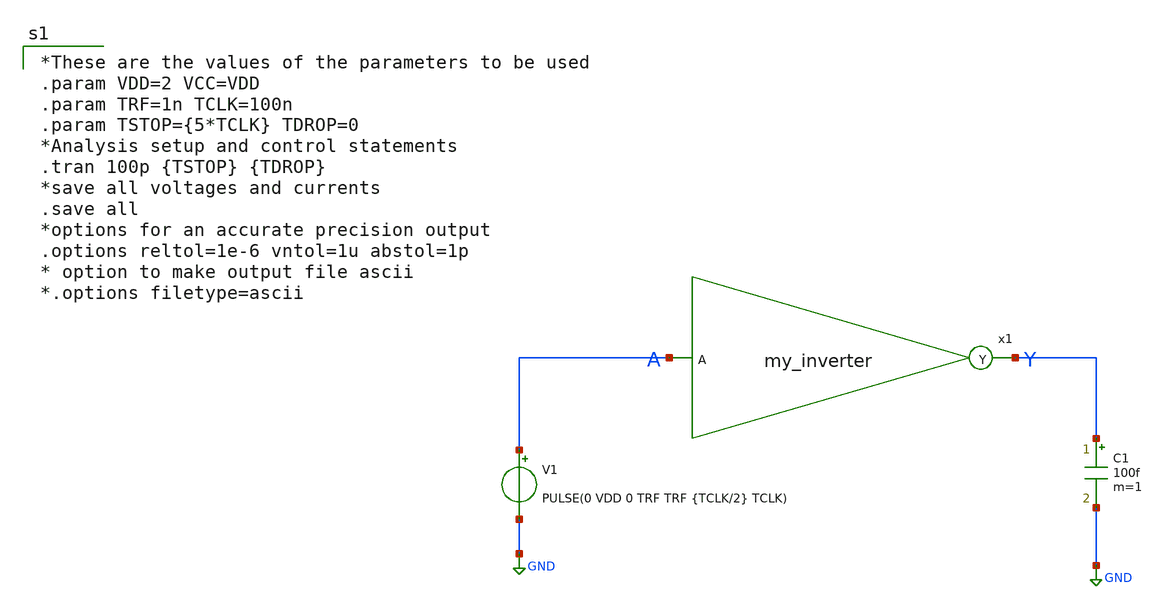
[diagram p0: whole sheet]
** sch_path: Lab4_test_bench.sch
**.subckt Lab4_test_bench
V1 A GND PULSE(0 VDD 0 TRF TRF {TCLK/2} TCLK)
C1 Y GND 100f m=1
x1 Y A my_inverter
**** begin user architecture code

*These are the values of the parameters to be used
.param VDD=2 VCC=VDD
.param TRF=1n TCLK=100n
.param TSTOP={5*TCLK} TDROP=0
*Analysis setup and control statements
.tran 100p {TSTOP} {TDROP}
*save all voltages and currents
.save all
*options for an accurate precision output
.options reltol=1e-6 vntol=1u abstol=1p
* option to make output file ascii
*.options filetype=ascii


**** end user architecture code
**.ends

* expanding   symbol:  my_inverter.sym # of pins=2
** sym_path: my_inverter.sym
** sch_path: my_inverter.sch
.subckt my_inverter Y A
*.ipin A
*.opin Y
**** begin user architecture code

a1 A Yi inv1
.model inv1 d_inverter(rise_delay = 0.5e-9 fall_delay = 0.5e-9 input_load = 0.1e-12)
v1 Yi Y 0


**** end user architecture code
.ends

.GLOBAL GND
.end
